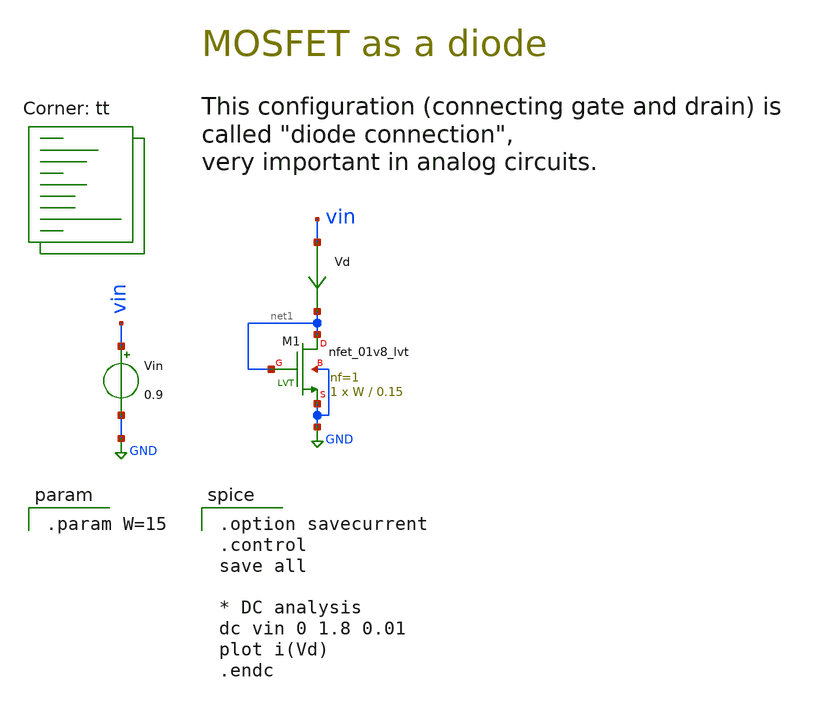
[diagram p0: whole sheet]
** sch_path: 00-e_diode.sch
**.subckt 00-e_diode
XM1 net1 net1 GND GND sky130_fd_pr__nfet_01v8_lvt L=0.15 W=W nf=1 ad='int((1 + 1)/2) * W / 1 * 0.29'
+ as='int((1 + 2)/2) * W / 1 * 0.29' pd='2*int((1 + 1)/2) * (W / 1 + 0.29)' ps='2*int((1 + 2)/2) * (W / 1 + 0.29)'
+ nrd='0.29 / W ' nrs='0.29 / W ' sa=0 sb=0 sd=0 mult=1 m=1
Vin vin GND 0.9
Vd vin net1 0
.save i(vd)
**** begin user architecture code
.lib $::SKYWATER_MODELS/sky130.lib.spice tt

.param W=15


.option savecurrent
.control
save all

* DC analysis
dc vin 0 1.8 0.01
plot i(Vd)
.endc

**** end user architecture code
**.ends
.GLOBAL GND
.end
